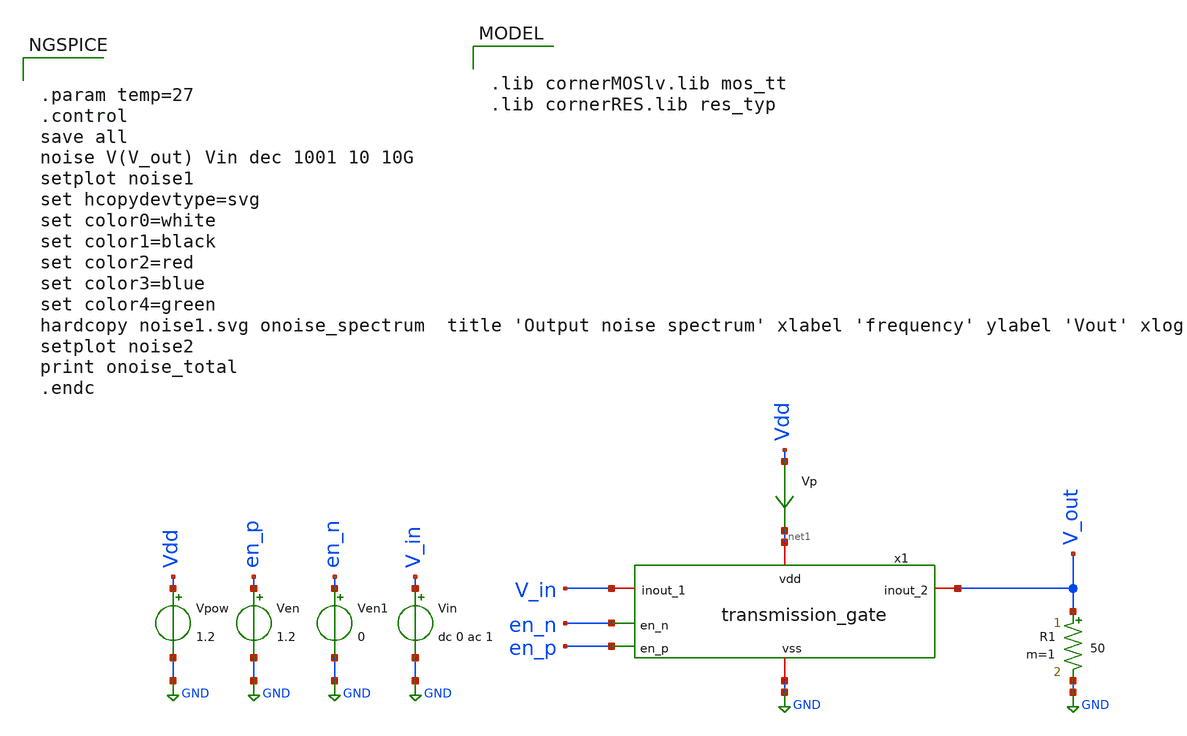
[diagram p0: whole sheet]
** sch_path: CHIPCHILE_CANELOS24_WorkshopTO/design_data/xschem/tgate/transmission_gate_tb_noise.sch
* Copyright 2023 IHP PDK Authors
**.subckt transmission_gate_tb_noise
Vpow Vdd GND 1.2
Vp Vdd net1 0
.save i(vp)
Vin V_in GND dc 0 ac 1
Ven en_p GND 1.2
Ven1 en_n GND 0
x1 net1 en_n V_in V_out en_p GND transmission_gate
R1 V_out GND 50 m=1
**** begin user architecture code

.lib cornerMOSlv.lib mos_tt
.lib cornerRES.lib res_typ



.param temp=27
.control
save all
noise V(V_out) Vin dec 1001 10 10G
setplot noise1
set hcopydevtype=svg
set color0=white
set color1=black
set color2=red
set color3=blue
set color4=green
hardcopy noise1.svg onoise_spectrum  title 'Output noise spectrum' xlabel 'frequency' ylabel 'Vout' xlog
setplot noise2
print onoise_total
.endc


**** end user architecture code
**.ends

* expanding   symbol:  transmission_gate.sym # of pins=6
** sym_path: CHIPCHILE_CANELOS24_WorkshopTO/design_data/xschem/multiplexer/transmission_gate.sym
** sch_path: CHIPCHILE_CANELOS24_WorkshopTO/design_data/xschem/multiplexer/transmission_gate.sch
.subckt transmission_gate vdd en_n inout_1 inout_2 en_p vss
*.iopin inout_1
*.iopin inout_2
*.ipin en_p
*.iopin vdd
*.iopin vss
*.ipin en_n
XM1 inout_1 en_p inout_2 net1 sg13_lv_nmos w=200.0u l=0.130u ng=20 m=1 mm_ok=1
XM2 inout_1 en_n inout_2 net2 sg13_lv_pmos w=200.0u l=0.130u ng=20 m=1 mm_ok=1
XR1 vdd net2 ntap1 R=262.8 w=0.78e-6 l=0.78e-6
XR2 vss net1 ptap1 R=262.8 w=0.78e-6 l=0.78e-6
.ends

.GLOBAL GND
.end
